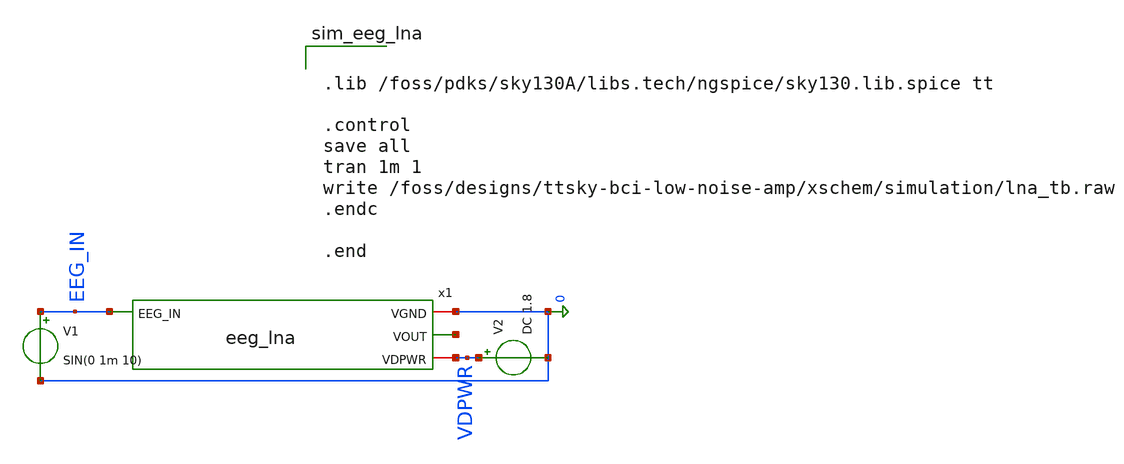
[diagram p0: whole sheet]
** sch_path: xschem/eeg_lna_tb.sch
**.subckt eeg_lna_tb
x1 EEG_IN 0 net1 VDPWR eeg_lna
V1 EEG_IN 0 SIN(0 1m 10)
V2 VDPWR 0 DC 1.8
**** begin user architecture code


.lib /foss/pdks/sky130A/libs.tech/ngspice/sky130.lib.spice tt

.control
save all
tran 1m 1
write /foss/designs/ttsky-bci-low-noise-amp/xschem/simulation/lna_tb.raw
.endc

.end


**** end user architecture code
**.ends

* expanding   symbol:  /foss/designs/ttsky-bci-low-noise-amp/xschem/eeg_lna.sym # of pins=4
** sym_path: xschem/eeg_lna.sym
** sch_path: xschem/eeg_lna.sch
.subckt eeg_lna EEG_IN VGND VOUT VDPWR
*.iopin VGND
*.ipin EEG_IN
*.iopin VDPWR
*.opin VOUT
XM1 net1 net1 VGND VGND sky130_fd_pr__nfet_01v8 L=1.0 W=1 nf=1 ad='int((1 + 1)/2) * 1 / 1 * 0.29' as='int((1 + 2)/2) * 1 / 1 * 0.29'
+ pd='2*int((1 + 1)/2) * (1 / 1 + 0.29)' ps='2*int((1 + 2)/2) * (1 / 1 + 0.29)' nrd='0.29 / 1 ' nrs='0.29 / 1 '
+ sa=0 sb=0 sd=0 mult=1 m=1
XM2 VOUT net1 VGND VGND sky130_fd_pr__nfet_01v8 L=1.0 W=1 nf=1 ad='int((1 + 1)/2) * 1 / 1 * 0.29' as='int((1 + 2)/2) * 1 / 1 * 0.29'
+ pd='2*int((1 + 1)/2) * (1 / 1 + 0.29)' ps='2*int((1 + 2)/2) * (1 / 1 + 0.29)' nrd='0.29 / 1 ' nrs='0.29 / 1 '
+ sa=0 sb=0 sd=0 mult=1 m=1
XM3 net1 net3 net2 VDPWR sky130_fd_pr__pfet_01v8 L=1.0 W=1 nf=1 ad='int((1 + 1)/2) * 1 / 1 * 0.29' as='int((1 + 2)/2) * 1 / 1 * 0.29'
+ pd='2*int((1 + 1)/2) * (1 / 1 + 0.29)' ps='2*int((1 + 2)/2) * (1 / 1 + 0.29)' nrd='0.29 / 1 ' nrs='0.29 / 1 '
+ sa=0 sb=0 sd=0 mult=1 m=1
XM4 VOUT net4 net2 VDPWR sky130_fd_pr__pfet_01v8 L=1.0 W=1 nf=1 ad='int((1 + 1)/2) * 1 / 1 * 0.29' as='int((1 + 2)/2) * 1 / 1 * 0.29'
+ pd='2*int((1 + 1)/2) * (1 / 1 + 0.29)' ps='2*int((1 + 2)/2) * (1 / 1 + 0.29)' nrd='0.29 / 1 ' nrs='0.29 / 1 '
+ sa=0 sb=0 sd=0 mult=1 m=1
XM5 net2 BIAS_P VDPWR VDPWR sky130_fd_pr__pfet_01v8 L=1.0 W=1 nf=1 ad='int((1 + 1)/2) * 1 / 1 * 0.29'
+ as='int((1 + 2)/2) * 1 / 1 * 0.29' pd='2*int((1 + 1)/2) * (1 / 1 + 0.29)' ps='2*int((1 + 2)/2) * (1 / 1 + 0.29)'
+ nrd='0.29 / 1 ' nrs='0.29 / 1 ' sa=0 sb=0 sd=0 mult=1 m=1
XM6 BIAS_P BIAS_P VDPWR VDPWR sky130_fd_pr__pfet_01v8 L=1.0 W=1 nf=1 ad='int((1 + 1)/2) * 1 / 1 * 0.29'
+ as='int((1 + 2)/2) * 1 / 1 * 0.29' pd='2*int((1 + 1)/2) * (1 / 1 + 0.29)' ps='2*int((1 + 2)/2) * (1 / 1 + 0.29)'
+ nrd='0.29 / 1 ' nrs='0.29 / 1 ' sa=0 sb=0 sd=0 mult=1 m=1
XM7 BIAS_P BIAS_P VGND VGND sky130_fd_pr__nfet_01v8 L=1.0 W=1 nf=1 ad='int((1 + 1)/2) * 1 / 1 * 0.29'
+ as='int((1 + 2)/2) * 1 / 1 * 0.29' pd='2*int((1 + 1)/2) * (1 / 1 + 0.29)' ps='2*int((1 + 2)/2) * (1 / 1 + 0.29)'
+ nrd='0.29 / 1 ' nrs='0.29 / 1 ' sa=0 sb=0 sd=0 mult=1 m=1
XCIN net3 EEG_IN sky130_fd_pr__cap_mim_m3_1 W=1 L=1 MF=1 m=1
RBIAS net3 BIAS_P 1Gig m=1
RF VOUT net4 1Meg m=1
RG net4 BIAS_P 10k m=1
.ends

.end
